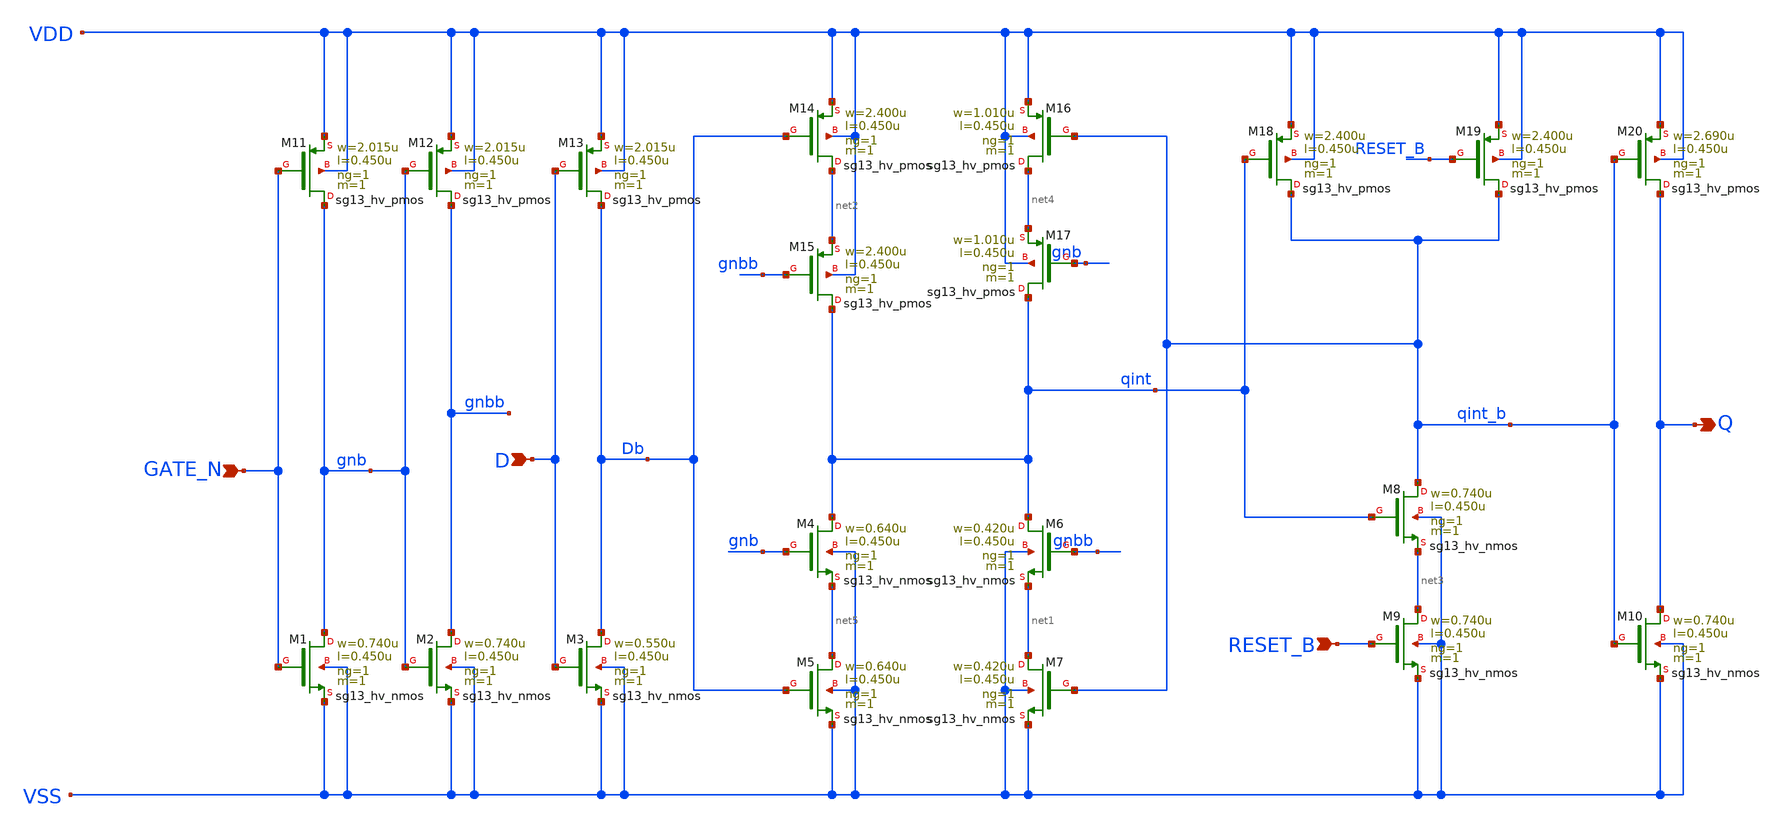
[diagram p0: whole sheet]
** sch_path: ihp-sg13g2/libs.ref/sg13g2_stdcell_hv/sch/xschem/sg13g2_hv_dllrq_1.sch
* Copyright 2023 IHP PDK Authors
* Licensed under the Apache License, Version 2.0 (the "License");
* you may not use this file except in compliance with the License.
* You may obtain a copy of the License at
* https://www.apache.org/licenses/LICENSE-2.0
* Unless required by applicable law or agreed to in writing, software
* distributed under the License is distributed on an "AS IS" BASIS,
* WITHOUT WARRANTIES OR CONDITIONS OF ANY KIND, either express or implied.
* See the License for the specific language governing permissions and
* limitations under the License.
**.subckt sg13g2_hv_dllrq_1 D GATE_N RESET_B Q
*.ipin D
*.ipin GATE_N
*.ipin RESET_B
*.opin Q
XM1 gnb GATE_N VSS VSS sg13_hv_nmos w=0.740u l=0.450u ng=1 m=1 mm_ok=1
XM2 gnbb gnb VSS VSS sg13_hv_nmos w=0.740u l=0.450u ng=1 m=1 mm_ok=1
XM3 Db D VSS VSS sg13_hv_nmos w=0.550u l=0.450u ng=1 m=1 mm_ok=1
XM4 qint gnb net5 VSS sg13_hv_nmos w=0.640u l=0.450u ng=1 m=1 mm_ok=1
XM5 net5 Db VSS VSS sg13_hv_nmos w=0.640u l=0.450u ng=1 m=1 mm_ok=1
XM6 qint gnbb net1 VSS sg13_hv_nmos w=0.420u l=0.450u ng=1 m=1 mm_ok=1
XM7 net1 qint_b VSS VSS sg13_hv_nmos w=0.420u l=0.450u ng=1 m=1 mm_ok=1
XM8 qint_b qint net3 VSS sg13_hv_nmos w=0.740u l=0.450u ng=1 m=1 mm_ok=1
XM9 net3 RESET_B VSS VSS sg13_hv_nmos w=0.740u l=0.450u ng=1 m=1 mm_ok=1
XM10 Q qint_b VSS VSS sg13_hv_nmos w=0.740u l=0.450u ng=1 m=1 mm_ok=1
XM11 gnb GATE_N VDD VDD sg13_hv_pmos w=2.015u l=0.450u ng=1 m=1 mm_ok=1
XM12 gnbb gnb VDD VDD sg13_hv_pmos w=2.015u l=0.450u ng=1 m=1 mm_ok=1
XM13 Db D VDD VDD sg13_hv_pmos w=2.015u l=0.450u ng=1 m=1 mm_ok=1
XM14 net2 Db VDD VDD sg13_hv_pmos w=2.400u l=0.450u ng=1 m=1 mm_ok=1
XM15 qint gnbb net2 VDD sg13_hv_pmos w=2.400u l=0.450u ng=1 m=1 mm_ok=1
XM16 net4 qint_b VDD VDD sg13_hv_pmos w=1.010u l=0.450u ng=1 m=1 mm_ok=1
XM17 qint gnb net4 VDD sg13_hv_pmos w=1.010u l=0.450u ng=1 m=1 mm_ok=1
XM18 qint_b qint VDD VDD sg13_hv_pmos w=2.400u l=0.450u ng=1 m=1 mm_ok=1
XM19 qint_b RESET_B VDD VDD sg13_hv_pmos w=2.400u l=0.450u ng=1 m=1 mm_ok=1
XM20 Q qint_b VDD VDD sg13_hv_pmos w=2.690u l=0.450u ng=1 m=1 mm_ok=1
**.ends
.end
